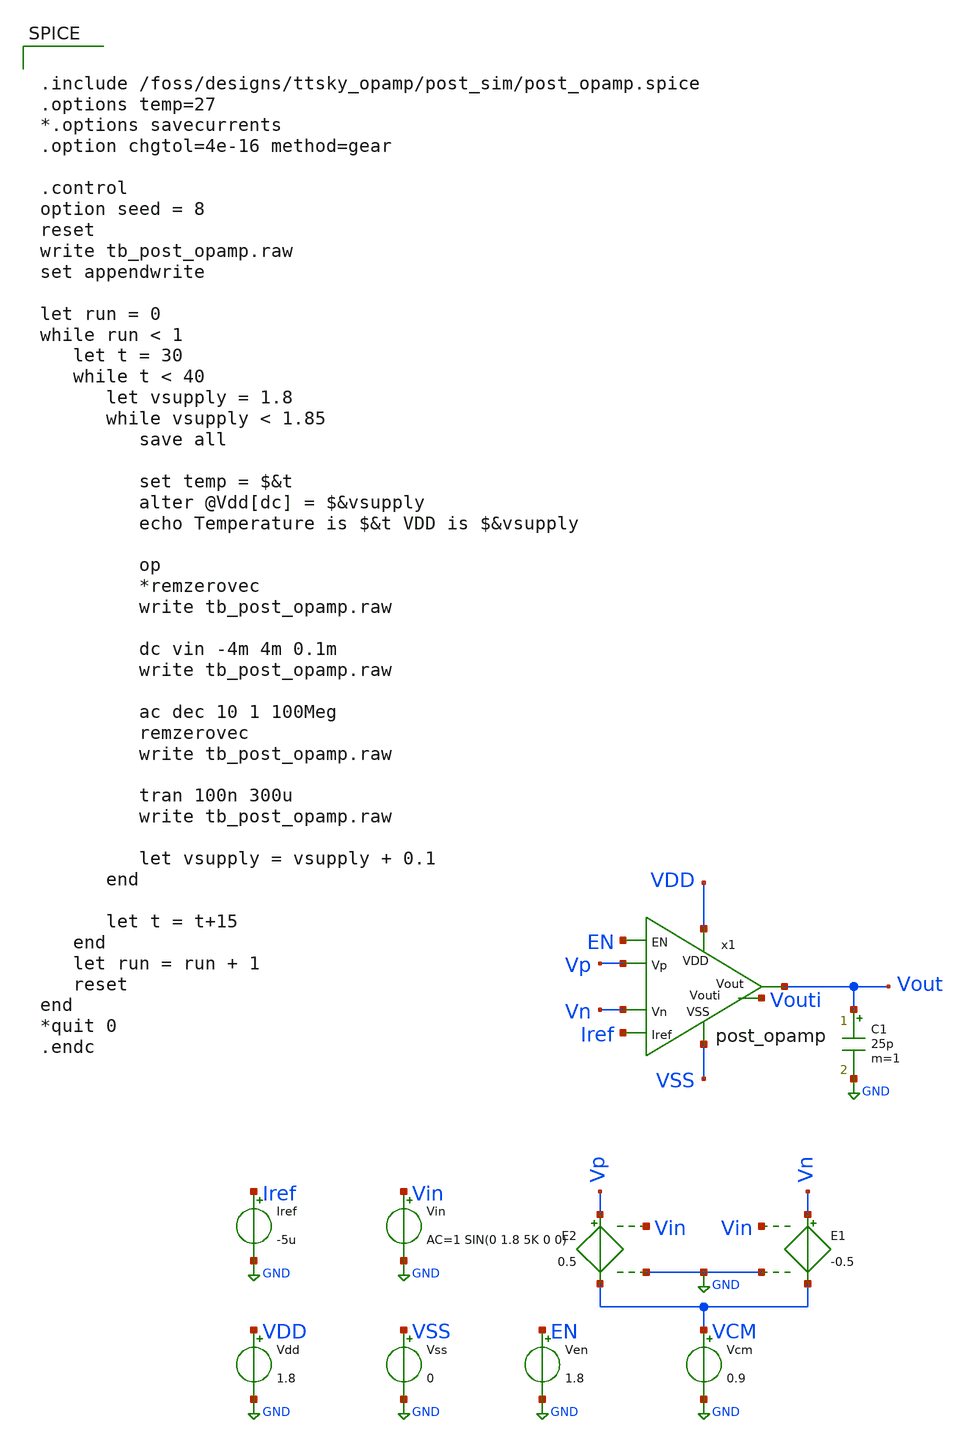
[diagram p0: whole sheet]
** sch_path: xschem/tb_post_opamp.sch
**.subckt tb_post_opamp
Vdd VDD GND 1.8
Vss VSS GND 0
E1 Vn VCM Vin GND -0.5
Vcm VCM GND 0.9
E2 Vp VCM Vin GND 0.5
Vin Vin GND AC=1 SIN(0 1.8 5K 0 0)
Iref Iref GND -5u
Ven EN GND 1.8
C1 Vout GND 25p m=1
x1 Vout Vn Vp VSS Iref VDD Vouti EN post_opamp
**** begin user architecture code


.include /foss/designs/ttsky_opamp/post_sim/post_opamp.spice
.options temp=27
*.options savecurrents
.option chgtol=4e-16 method=gear

.control
option seed = 8
reset
write tb_post_opamp.raw
set appendwrite

let run = 0
while run < 1
   let t = 30
   while t < 40
      let vsupply = 1.8
      while vsupply < 1.85
         save all

         set temp = $&t
         alter @Vdd[dc] = $&vsupply
         echo Temperature is $&t VDD is $&vsupply

         op
         *remzerovec
         write tb_post_opamp.raw

         dc vin -4m 4m 0.1m
         write tb_post_opamp.raw

         ac dec 10 1 100Meg
         remzerovec
         write tb_post_opamp.raw

         tran 100n 300u
         write tb_post_opamp.raw

         let vsupply = vsupply + 0.1
      end

      let t = t+15
   end
   let run = run + 1
   reset
end
*quit 0
.endc



** opencircuitdesign pdks install
.param MT_SWITCH = 1.0
.lib $::SKYWATER_MODELS/sky130.lib.spice tt

**** end user architecture code
**.ends
.GLOBAL GND
.end
